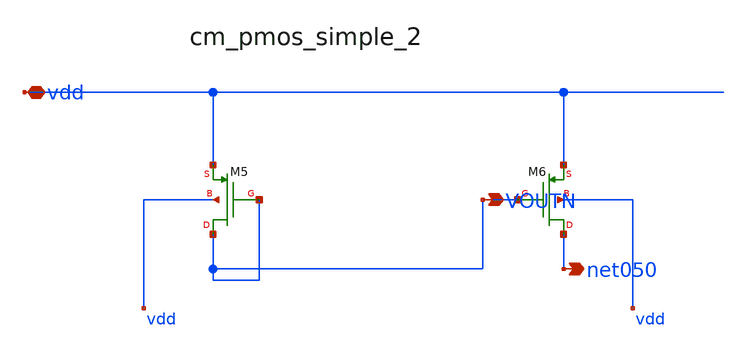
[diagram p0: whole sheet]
** sch_path: analog-db/raw/amp_002_alfio_raffc/hier/blocks/cm_pmos_simple_2.sch
**.subckt cm_pmos_simple_2 vdd VOUTN net050
*.iopin vdd
*.opin VOUTN
*.opin net050
XM5 VOUTN VOUTN vdd vdd sg13_lv_pmos w=x_dut_xm5_w l=x_dut_xm5_l ng=1 m=x_dut_xm5_m
XM6 net050 VOUTN vdd vdd sg13_lv_pmos w=x_dut_xm6_w l=x_dut_xm6_l ng=1 m=x_dut_xm6_m
**.ends
.end
